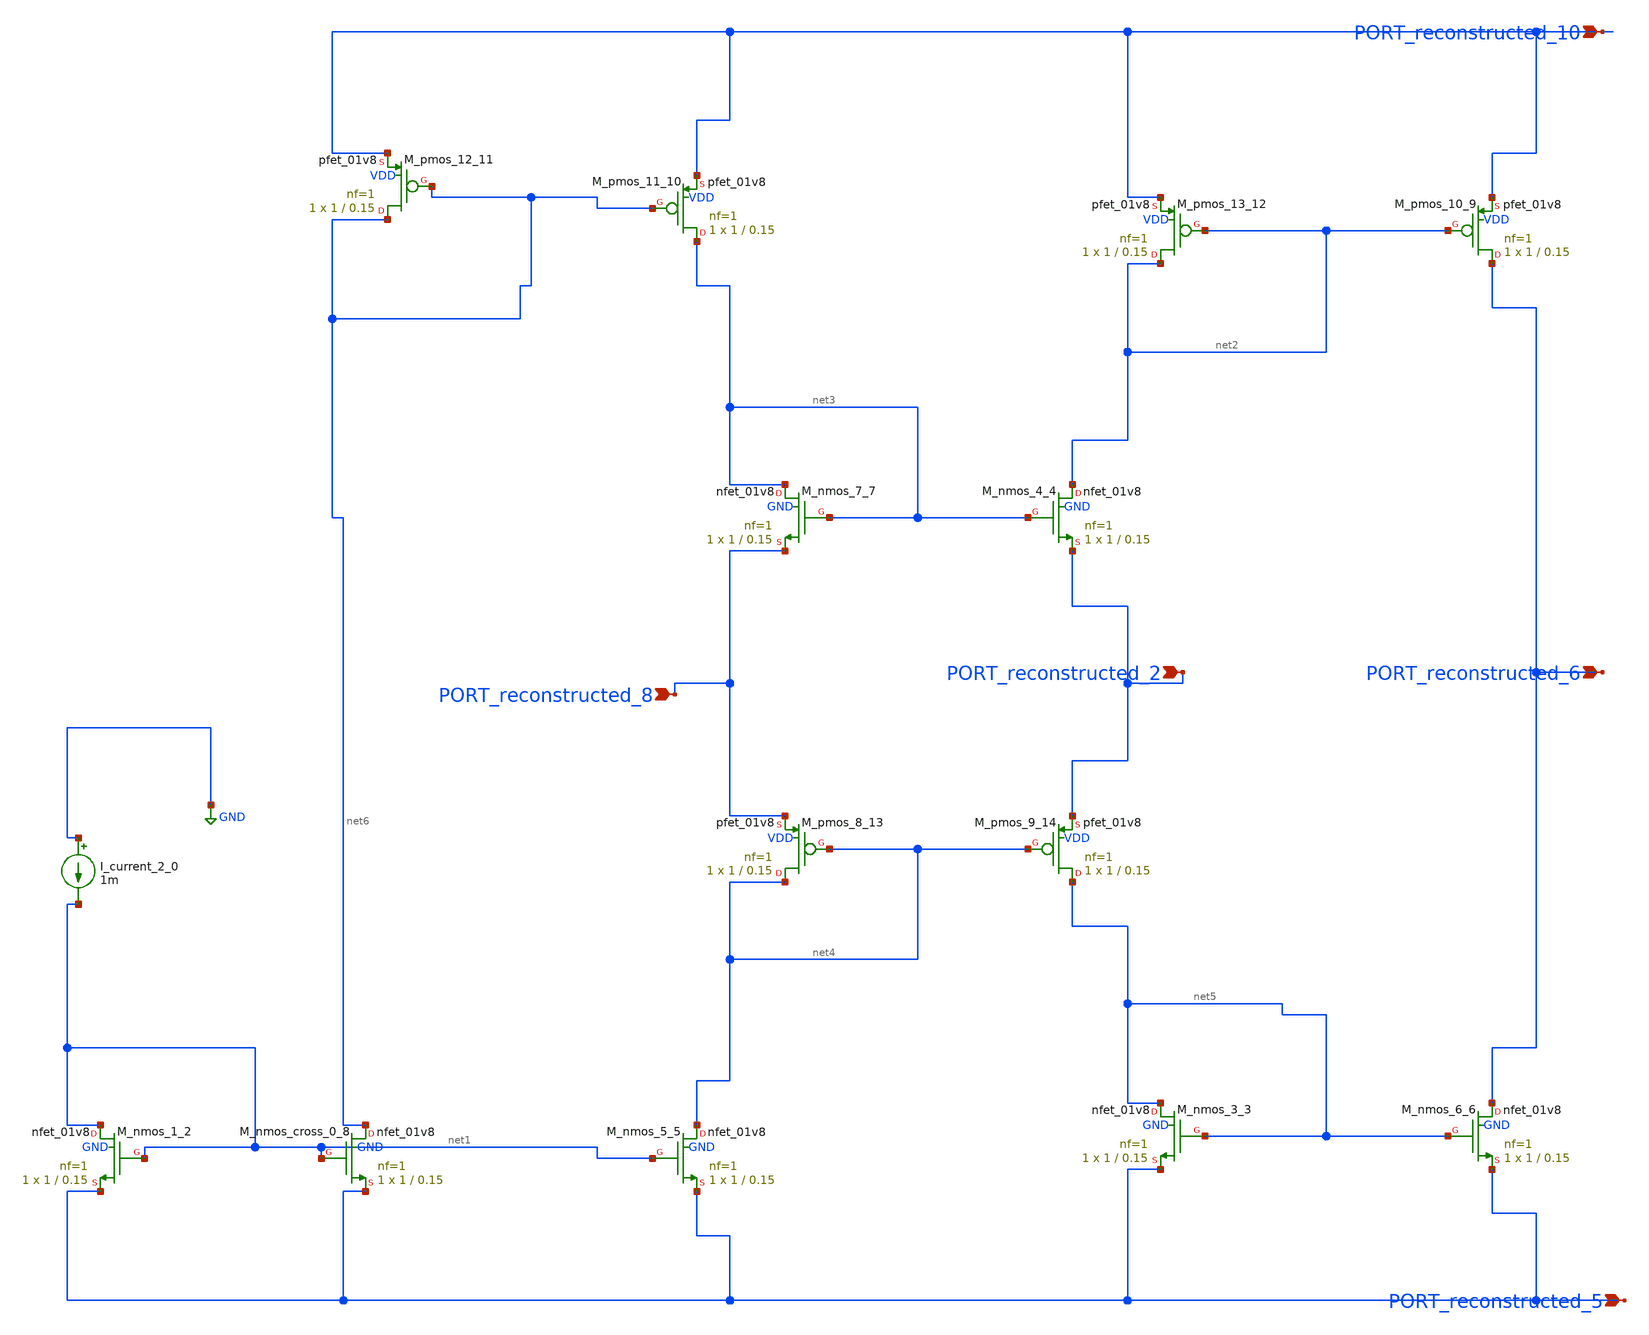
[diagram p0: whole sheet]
** sch_path: schematics/p06_fig1f_cccii.sch
**.subckt p06_fig1f_cccii PORT_reconstructed_8 PORT_reconstructed_2 PORT_reconstructed_6
*+ PORT_reconstructed_5 PORT_reconstructed_10
*.ipin PORT_reconstructed_8
*.ipin PORT_reconstructed_2
*.ipin PORT_reconstructed_6
*.ipin PORT_reconstructed_5
*.ipin PORT_reconstructed_10
I_current_2_0 GND net1 1m
XM_nmos_1_2 net1 net1 PORT_reconstructed_5 GND sky130_fd_pr__nfet_01v8 L=0.15 W=1 nf=1 ad='int((1 + 1)/2) * 1 / 1 * 0.29'
+ as='int((1 + 2)/2) * 1 / 1 * 0.29' pd='2*int((1 + 1)/2) * (1 / 1 + 0.29)' ps='2*int((1 + 2)/2) * (1 / 1 + 0.29)'
+ nrd='0.29 / 1 ' nrs='0.29 / 1 ' sa=0 sb=0 sd=0 mult=1 m=1
XM_nmos_3_3 net5 net5 PORT_reconstructed_5 GND sky130_fd_pr__nfet_01v8 L=0.15 W=1 nf=1 ad='int((1 + 1)/2) * 1 / 1 * 0.29'
+ as='int((1 + 2)/2) * 1 / 1 * 0.29' pd='2*int((1 + 1)/2) * (1 / 1 + 0.29)' ps='2*int((1 + 2)/2) * (1 / 1 + 0.29)'
+ nrd='0.29 / 1 ' nrs='0.29 / 1 ' sa=0 sb=0 sd=0 mult=1 m=1
XM_nmos_4_4 net2 net3 PORT_reconstructed_2 GND sky130_fd_pr__nfet_01v8 L=0.15 W=1 nf=1 ad='int((1 + 1)/2) * 1 / 1 * 0.29'
+ as='int((1 + 2)/2) * 1 / 1 * 0.29' pd='2*int((1 + 1)/2) * (1 / 1 + 0.29)' ps='2*int((1 + 2)/2) * (1 / 1 + 0.29)'
+ nrd='0.29 / 1 ' nrs='0.29 / 1 ' sa=0 sb=0 sd=0 mult=1 m=1
XM_nmos_5_5 net4 net1 PORT_reconstructed_5 GND sky130_fd_pr__nfet_01v8 L=0.15 W=1 nf=1 ad='int((1 + 1)/2) * 1 / 1 * 0.29'
+ as='int((1 + 2)/2) * 1 / 1 * 0.29' pd='2*int((1 + 1)/2) * (1 / 1 + 0.29)' ps='2*int((1 + 2)/2) * (1 / 1 + 0.29)'
+ nrd='0.29 / 1 ' nrs='0.29 / 1 ' sa=0 sb=0 sd=0 mult=1 m=1
XM_nmos_6_6 PORT_reconstructed_6 net5 PORT_reconstructed_5 GND sky130_fd_pr__nfet_01v8 L=0.15 W=1 nf=1
+ ad='int((1 + 1)/2) * 1 / 1 * 0.29' as='int((1 + 2)/2) * 1 / 1 * 0.29' pd='2*int((1 + 1)/2) * (1 / 1 + 0.29)'
+ ps='2*int((1 + 2)/2) * (1 / 1 + 0.29)' nrd='0.29 / 1 ' nrs='0.29 / 1 ' sa=0 sb=0 sd=0 mult=1 m=1
XM_nmos_7_7 net3 net3 PORT_reconstructed_8 GND sky130_fd_pr__nfet_01v8 L=0.15 W=1 nf=1 ad='int((1 + 1)/2) * 1 / 1 * 0.29'
+ as='int((1 + 2)/2) * 1 / 1 * 0.29' pd='2*int((1 + 1)/2) * (1 / 1 + 0.29)' ps='2*int((1 + 2)/2) * (1 / 1 + 0.29)'
+ nrd='0.29 / 1 ' nrs='0.29 / 1 ' sa=0 sb=0 sd=0 mult=1 m=1
XM_nmos_cross_0_8 net6 net1 PORT_reconstructed_5 GND sky130_fd_pr__nfet_01v8 L=0.15 W=1 nf=1 ad='int((1 + 1)/2) * 1 / 1 * 0.29'
+ as='int((1 + 2)/2) * 1 / 1 * 0.29' pd='2*int((1 + 1)/2) * (1 / 1 + 0.29)' ps='2*int((1 + 2)/2) * (1 / 1 + 0.29)'
+ nrd='0.29 / 1 ' nrs='0.29 / 1 ' sa=0 sb=0 sd=0 mult=1 m=1
XM_pmos_10_9 PORT_reconstructed_6 net2 PORT_reconstructed_10 VDD sky130_fd_pr__pfet_01v8 L=0.15 W=1 nf=1
+ ad='int((1 + 1)/2) * 1 / 1 * 0.29' as='int((1 + 2)/2) * 1 / 1 * 0.29' pd='2*int((1 + 1)/2) * (1 / 1 + 0.29)'
+ ps='2*int((1 + 2)/2) * (1 / 1 + 0.29)' nrd='0.29 / 1 ' nrs='0.29 / 1 ' sa=0 sb=0 sd=0 mult=1 m=1
XM_pmos_11_10 net3 net6 PORT_reconstructed_10 VDD sky130_fd_pr__pfet_01v8 L=0.15 W=1 nf=1 ad='int((1 + 1)/2) * 1 / 1 * 0.29'
+ as='int((1 + 2)/2) * 1 / 1 * 0.29' pd='2*int((1 + 1)/2) * (1 / 1 + 0.29)' ps='2*int((1 + 2)/2) * (1 / 1 + 0.29)'
+ nrd='0.29 / 1 ' nrs='0.29 / 1 ' sa=0 sb=0 sd=0 mult=1 m=1
XM_pmos_12_11 net6 net6 PORT_reconstructed_10 VDD sky130_fd_pr__pfet_01v8 L=0.15 W=1 nf=1 ad='int((1 + 1)/2) * 1 / 1 * 0.29'
+ as='int((1 + 2)/2) * 1 / 1 * 0.29' pd='2*int((1 + 1)/2) * (1 / 1 + 0.29)' ps='2*int((1 + 2)/2) * (1 / 1 + 0.29)'
+ nrd='0.29 / 1 ' nrs='0.29 / 1 ' sa=0 sb=0 sd=0 mult=1 m=1
XM_pmos_13_12 net2 net2 PORT_reconstructed_10 VDD sky130_fd_pr__pfet_01v8 L=0.15 W=1 nf=1 ad='int((1 + 1)/2) * 1 / 1 * 0.29'
+ as='int((1 + 2)/2) * 1 / 1 * 0.29' pd='2*int((1 + 1)/2) * (1 / 1 + 0.29)' ps='2*int((1 + 2)/2) * (1 / 1 + 0.29)'
+ nrd='0.29 / 1 ' nrs='0.29 / 1 ' sa=0 sb=0 sd=0 mult=1 m=1
XM_pmos_8_13 net4 net4 PORT_reconstructed_8 VDD sky130_fd_pr__pfet_01v8 L=0.15 W=1 nf=1 ad='int((1 + 1)/2) * 1 / 1 * 0.29'
+ as='int((1 + 2)/2) * 1 / 1 * 0.29' pd='2*int((1 + 1)/2) * (1 / 1 + 0.29)' ps='2*int((1 + 2)/2) * (1 / 1 + 0.29)'
+ nrd='0.29 / 1 ' nrs='0.29 / 1 ' sa=0 sb=0 sd=0 mult=1 m=1
XM_pmos_9_14 net5 net4 PORT_reconstructed_2 VDD sky130_fd_pr__pfet_01v8 L=0.15 W=1 nf=1 ad='int((1 + 1)/2) * 1 / 1 * 0.29'
+ as='int((1 + 2)/2) * 1 / 1 * 0.29' pd='2*int((1 + 1)/2) * (1 / 1 + 0.29)' ps='2*int((1 + 2)/2) * (1 / 1 + 0.29)'
+ nrd='0.29 / 1 ' nrs='0.29 / 1 ' sa=0 sb=0 sd=0 mult=1 m=1
**.ends
.GLOBAL GND
.end
